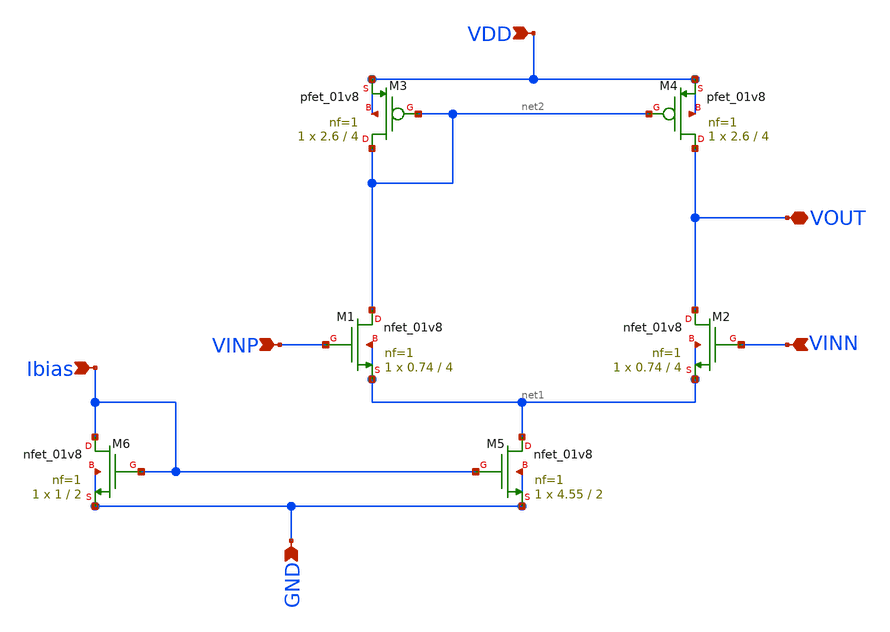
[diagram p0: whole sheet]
** sch_path: low_power/5tota_lowpower.sch
**.subckt 5tota_lowpower VDD VOUT VINN VINP Ibias GND
*.ipin VDD
*.iopin VOUT
*.ipin VINN
*.ipin VINP
*.ipin Ibias
*.ipin GND
XM1 net2 VINP net1 net1 sky130_fd_pr__nfet_01v8 L=4 W=0.74 nf=1 ad='int((1 + 1)/2) * 0.74 / 1 * 0.29'
+ as='int((1 + 2)/2) * 0.74 / 1 * 0.29' pd='2*int((1 + 1)/2) * (0.74 / 1 + 0.29)' ps='2*int((1 + 2)/2) * (0.74 / 1 + 0.29)'
+ nrd='0.29 / 0.74 ' nrs='0.29 / 0.74 ' sa=0 sb=0 sd=0 mult=1 m=1
XM5 net1 Ibias GND GND sky130_fd_pr__nfet_01v8 L=2 W=4.55 nf=1 ad='int((1 + 1)/2) * 4.55 / 1 * 0.29'
+ as='int((1 + 2)/2) * 4.55 / 1 * 0.29' pd='2*int((1 + 1)/2) * (4.55 / 1 + 0.29)' ps='2*int((1 + 2)/2) * (4.55 / 1 + 0.29)'
+ nrd='0.29 / 4.55 ' nrs='0.29 / 4.55 ' sa=0 sb=0 sd=0 mult=1 m=1
XM2 VOUT VINN net1 net1 sky130_fd_pr__nfet_01v8 L=4 W=0.74 nf=1 ad='int((1 + 1)/2) * 0.74 / 1 * 0.29'
+ as='int((1 + 2)/2) * 0.74 / 1 * 0.29' pd='2*int((1 + 1)/2) * (0.74 / 1 + 0.29)' ps='2*int((1 + 2)/2) * (0.74 / 1 + 0.29)'
+ nrd='0.29 / 0.74 ' nrs='0.29 / 0.74 ' sa=0 sb=0 sd=0 mult=1 m=1
XM3 net2 net2 VDD VDD sky130_fd_pr__pfet_01v8 L=4 W=2.6 nf=1 ad='int((1 + 1)/2) * 2.6 / 1 * 0.29' as='int((1 + 2)/2) * 2.6 / 1 * 0.29'
+ pd='2*int((1 + 1)/2) * (2.6 / 1 + 0.29)' ps='2*int((1 + 2)/2) * (2.6 / 1 + 0.29)' nrd='0.29 / 2.6 ' nrs='0.29 / 2.6 '
+ sa=0 sb=0 sd=0 mult=1 m=1
XM4 VOUT net2 VDD VDD sky130_fd_pr__pfet_01v8 L=4 W=2.6 nf=1 ad='int((1 + 1)/2) * 2.6 / 1 * 0.29' as='int((1 + 2)/2) * 2.6 / 1 * 0.29'
+ pd='2*int((1 + 1)/2) * (2.6 / 1 + 0.29)' ps='2*int((1 + 2)/2) * (2.6 / 1 + 0.29)' nrd='0.29 / 2.6 ' nrs='0.29 / 2.6 '
+ sa=0 sb=0 sd=0 mult=1 m=1
XM6 Ibias Ibias GND GND sky130_fd_pr__nfet_01v8 L=2 W=1 nf=1 ad='int((1 + 1)/2) * 1 / 1 * 0.29' as='int((1 + 2)/2) * 1 / 1 * 0.29'
+ pd='2*int((1 + 1)/2) * (1 / 1 + 0.29)' ps='2*int((1 + 2)/2) * (1 / 1 + 0.29)' nrd='0.29 / 1 ' nrs='0.29 / 1 '
+ sa=0 sb=0 sd=0 mult=1 m=1
**.ends
.end
